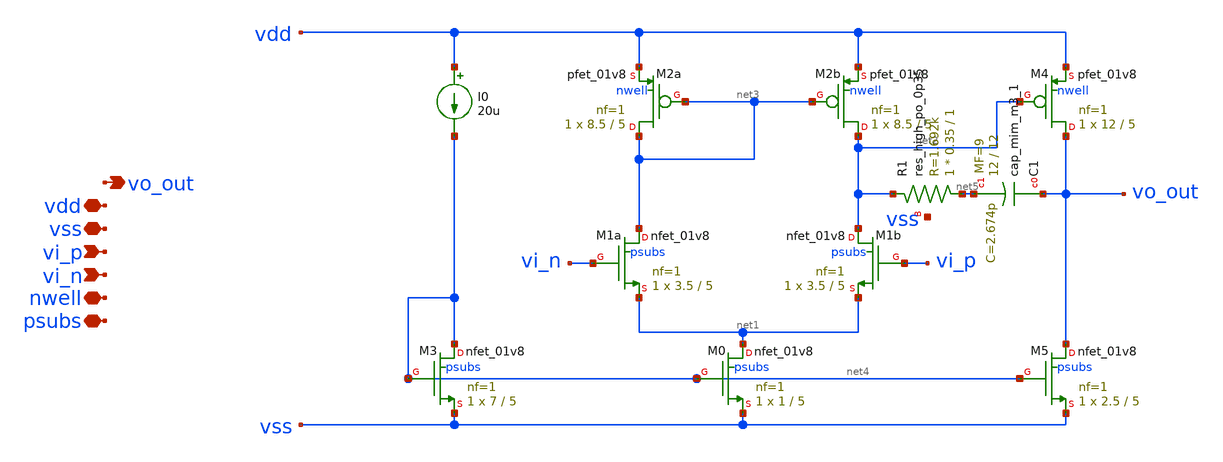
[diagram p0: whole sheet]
** sch_path: xschem/op.sch
**.subckt op vss vdd vo_out vi_p vi_n psubs nwell
*.iopin vss
*.iopin vdd
*.opin vo_out
*.ipin vi_p
*.ipin vi_n
*.iopin psubs
*.iopin nwell
XM1a net3 vi_n net1 psubs sky130_fd_pr__nfet_01v8 L=5 W=3.5 nf=1 ad='int((nf+1)/2) * W/nf * 0.29' as='int((nf+2)/2) * W/nf * 0.29'
+ pd='2*int((nf+1)/2) * (W/nf + 0.29)' ps='2*int((nf+2)/2) * (W/nf + 0.29)' nrd='0.29 / W' nrs='0.29 / W'
+ sa=0 sb=0 sd=0 mult=1 m=1
XM2a net3 net3 vdd nwell sky130_fd_pr__pfet_01v8 L=5 W=8.5 nf=1 ad='int((1 + 1)/2) * 8.5 / 1 * 0.29'
+ as='int((1 + 2)/2) * 8.5 / 1 * 0.29' pd='2*int((1 + 1)/2) * (8.5 / 1 + 0.29)' ps='2*int((1 + 2)/2) * (8.5 / 1 + 0.29)'
+ nrd='0.29 / 8.5 ' nrs='0.29 / 8.5 ' sa=0 sb=0 sd=0 mult=1 m=1
XM3 net4 net4 vss psubs sky130_fd_pr__nfet_01v8 L=5 W=7 nf=1 ad='int((1 + 1)/2) * 7 / 1 * 0.29' as='int((1 + 2)/2) * 7 / 1 * 0.29'
+ pd='2*int((1 + 1)/2) * (7 / 1 + 0.29)' ps='2*int((1 + 2)/2) * (7 / 1 + 0.29)' nrd='0.29 / 7 ' nrs='0.29 / 7 '
+ sa=0 sb=0 sd=0 mult=1 m=1
XM0 net1 net4 vss psubs sky130_fd_pr__nfet_01v8 L=5 W=1 nf=1 ad='int((1 + 1)/2) * 1 / 1 * 0.29' as='int((1 + 2)/2) * 1 / 1 * 0.29'
+ pd='2*int((1 + 1)/2) * (1 / 1 + 0.29)' ps='2*int((1 + 2)/2) * (1 / 1 + 0.29)' nrd='0.29 / 1 ' nrs='0.29 / 1 '
+ sa=0 sb=0 sd=0 mult=1 m=1
XM4 vo_out net2 vdd nwell sky130_fd_pr__pfet_01v8 L=5 W=12 nf=1 ad='int((1 + 1)/2) * 12 / 1 * 0.29' as='int((1 + 2)/2) * 12 / 1 * 0.29'
+ pd='2*int((1 + 1)/2) * (12 / 1 + 0.29)' ps='2*int((1 + 2)/2) * (12 / 1 + 0.29)' nrd='0.29 / 12 ' nrs='0.29 / 12 '
+ sa=0 sb=0 sd=0 mult=1 m=1
XM5 vo_out net4 vss psubs sky130_fd_pr__nfet_01v8 L=5 W=2.5 nf=1 ad='int((1 + 1)/2) * 2.5 / 1 * 0.29'
+ as='int((1 + 2)/2) * 2.5 / 1 * 0.29' pd='2*int((1 + 1)/2) * (2.5 / 1 + 0.29)' ps='2*int((1 + 2)/2) * (2.5 / 1 + 0.29)'
+ nrd='0.29 / 2.5 ' nrs='0.29 / 2.5 ' sa=0 sb=0 sd=0 mult=1 m=1
XM1b net2 vi_p net1 psubs sky130_fd_pr__nfet_01v8 L=5 W=3.5 nf=1 ad='int((nf+1)/2) * W/nf * 0.29' as='int((nf+2)/2) * W/nf * 0.29'
+ pd='2*int((nf+1)/2) * (W/nf + 0.29)' ps='2*int((nf+2)/2) * (W/nf + 0.29)' nrd='0.29 / W' nrs='0.29 / W'
+ sa=0 sb=0 sd=0 mult=1 m=1
XM2b net2 net3 vdd nwell sky130_fd_pr__pfet_01v8 L=5 W=8.5 nf=1 ad='int((1 + 1)/2) * 8.5 / 1 * 0.29'
+ as='int((1 + 2)/2) * 8.5 / 1 * 0.29' pd='2*int((1 + 1)/2) * (8.5 / 1 + 0.29)' ps='2*int((1 + 2)/2) * (8.5 / 1 + 0.29)'
+ nrd='0.29 / 8.5 ' nrs='0.29 / 8.5 ' sa=0 sb=0 sd=0 mult=1 m=1
XC1 vo_out net5 sky130_fd_pr__cap_mim_m3_1 W=12 L=12 MF=9 m=9
XR1 net5 net2 vss sky130_fd_pr__res_high_po_0p35 L=1 mult=1 m=1
I0 vdd net4 20u
**.ends
.end
